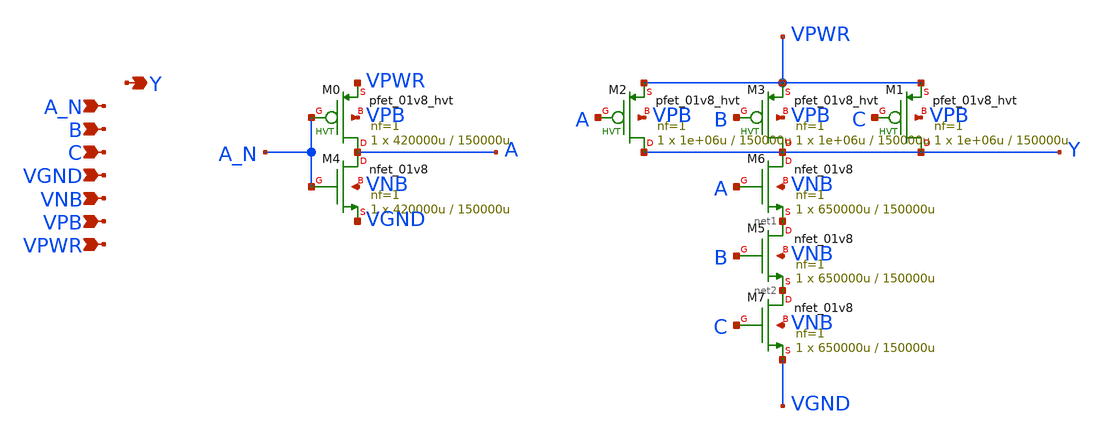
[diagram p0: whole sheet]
** sch_path: schematics/nand3b/sky130_fd_sc_hd__nand3b_1.sch
**.subckt sky130_fd_sc_hd__nand3b_1 A_N B C VGND VNB VPB VPWR Y
*.ipin A_N
*.ipin B
*.ipin C
*.ipin VGND
*.ipin VNB
*.ipin VPB
*.ipin VPWR
*.opin Y
XM0 A A_N VPWR VPB sky130_fd_pr__pfet_01v8_hvt L=150000u W=420000u nf=1 ad='int((1 + 1)/2) * 420000u / 1 * 0.29'
+ as='int((1 + 2)/2) * 420000u / 1 * 0.29' pd='2*int((1 + 1)/2) * (420000u / 1 + 0.29)' ps='2*int((1 + 2)/2) * (420000u / 1 + 0.29)'
+ nrd='0.29 / 420000u ' nrs='0.29 / 420000u ' sa=0 sb=0 sd=0 mult=1 m=1
XM1 Y C VPWR VPB sky130_fd_pr__pfet_01v8_hvt L=150000u W=1e+06u nf=1 ad='int((1 + 1)/2) * 1e+06u / 1 * 0.29'
+ as='int((1 + 2)/2) * 1e+06u / 1 * 0.29' pd='2*int((1 + 1)/2) * (1e+06u / 1 + 0.29)' ps='2*int((1 + 2)/2) * (1e+06u / 1 + 0.29)'
+ nrd='0.29 / 1e+06u ' nrs='0.29 / 1e+06u ' sa=0 sb=0 sd=0 mult=1 m=1
XM2 Y A VPWR VPB sky130_fd_pr__pfet_01v8_hvt L=150000u W=1e+06u nf=1 ad='int((1 + 1)/2) * 1e+06u / 1 * 0.29'
+ as='int((1 + 2)/2) * 1e+06u / 1 * 0.29' pd='2*int((1 + 1)/2) * (1e+06u / 1 + 0.29)' ps='2*int((1 + 2)/2) * (1e+06u / 1 + 0.29)'
+ nrd='0.29 / 1e+06u ' nrs='0.29 / 1e+06u ' sa=0 sb=0 sd=0 mult=1 m=1
XM3 Y B VPWR VPB sky130_fd_pr__pfet_01v8_hvt L=150000u W=1e+06u nf=1 ad='int((1 + 1)/2) * 1e+06u / 1 * 0.29'
+ as='int((1 + 2)/2) * 1e+06u / 1 * 0.29' pd='2*int((1 + 1)/2) * (1e+06u / 1 + 0.29)' ps='2*int((1 + 2)/2) * (1e+06u / 1 + 0.29)'
+ nrd='0.29 / 1e+06u ' nrs='0.29 / 1e+06u ' sa=0 sb=0 sd=0 mult=1 m=1
XM4 A A_N VGND VNB sky130_fd_pr__nfet_01v8 L=150000u W=420000u nf=1 ad='int((1 + 1)/2) * 420000u / 1 * 0.29'
+ as='int((1 + 2)/2) * 420000u / 1 * 0.29' pd='2*int((1 + 1)/2) * (420000u / 1 + 0.29)' ps='2*int((1 + 2)/2) * (420000u / 1 + 0.29)'
+ nrd='0.29 / 420000u ' nrs='0.29 / 420000u ' sa=0 sb=0 sd=0 mult=1 m=1
XM5 net1 B net2 VNB sky130_fd_pr__nfet_01v8 L=150000u W=650000u nf=1 ad='int((1 + 1)/2) * 650000u / 1 * 0.29'
+ as='int((1 + 2)/2) * 650000u / 1 * 0.29' pd='2*int((1 + 1)/2) * (650000u / 1 + 0.29)' ps='2*int((1 + 2)/2) * (650000u / 1 + 0.29)'
+ nrd='0.29 / 650000u ' nrs='0.29 / 650000u ' sa=0 sb=0 sd=0 mult=1 m=1
XM6 Y A net1 VNB sky130_fd_pr__nfet_01v8 L=150000u W=650000u nf=1 ad='int((1 + 1)/2) * 650000u / 1 * 0.29'
+ as='int((1 + 2)/2) * 650000u / 1 * 0.29' pd='2*int((1 + 1)/2) * (650000u / 1 + 0.29)' ps='2*int((1 + 2)/2) * (650000u / 1 + 0.29)'
+ nrd='0.29 / 650000u ' nrs='0.29 / 650000u ' sa=0 sb=0 sd=0 mult=1 m=1
XM7 net2 C VGND VNB sky130_fd_pr__nfet_01v8 L=150000u W=650000u nf=1 ad='int((1 + 1)/2) * 650000u / 1 * 0.29'
+ as='int((1 + 2)/2) * 650000u / 1 * 0.29' pd='2*int((1 + 1)/2) * (650000u / 1 + 0.29)' ps='2*int((1 + 2)/2) * (650000u / 1 + 0.29)'
+ nrd='0.29 / 650000u ' nrs='0.29 / 650000u ' sa=0 sb=0 sd=0 mult=1 m=1
**.ends
.end
